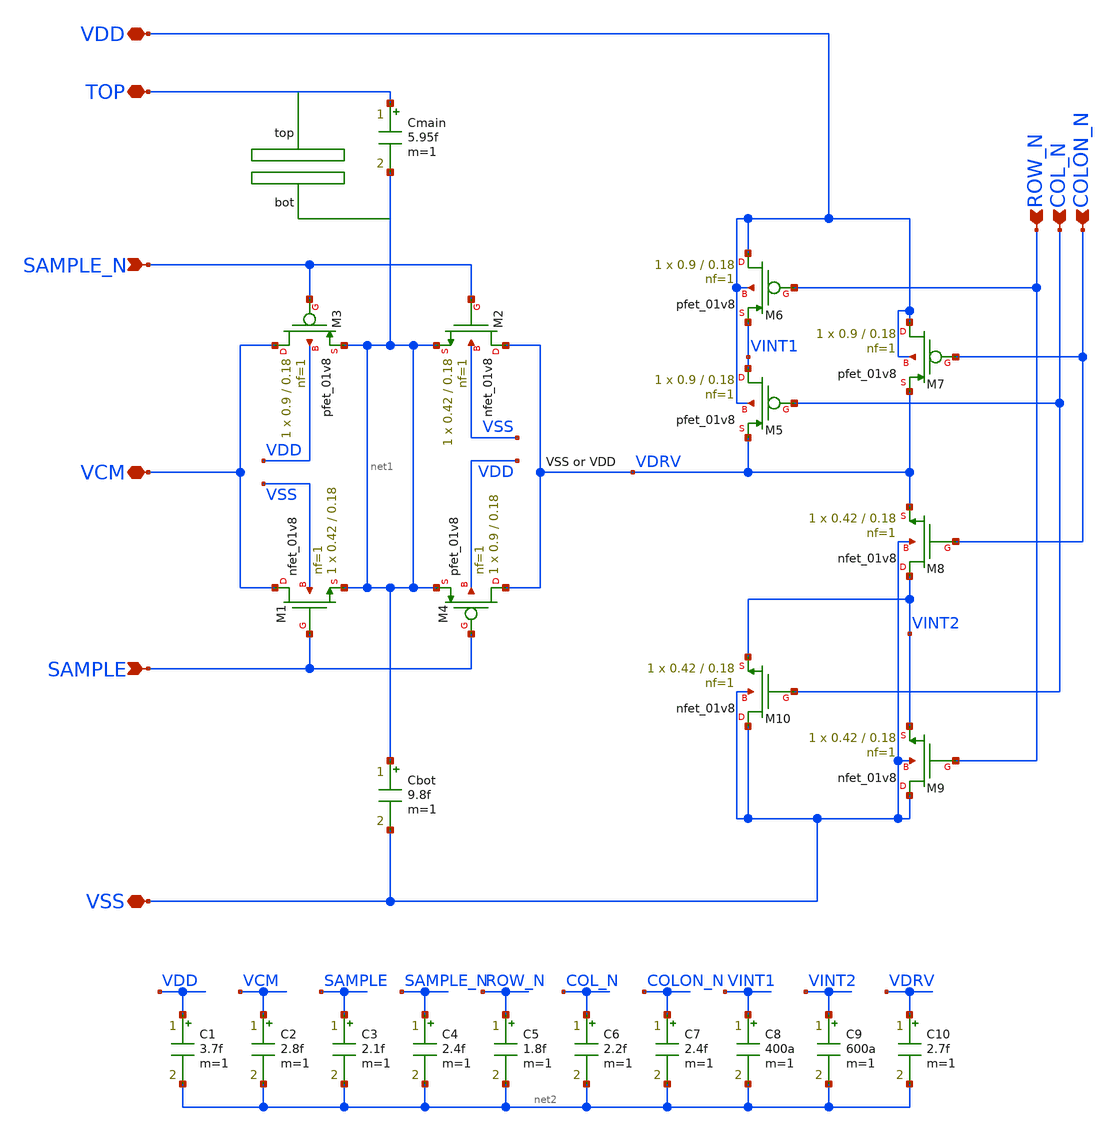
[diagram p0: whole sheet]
** sch_path: xschem/adc_array_cap/adc_array_cap_16.sch
**.subckt adc_array_cap_16 SAMPLE_N SAMPLE VCM ROW_N COL_N COLON_N VDD VSS TOP
*.ipin SAMPLE_N
*.ipin SAMPLE
*.iopin VCM
*.ipin ROW_N
*.ipin COL_N
*.ipin COLON_N
*.iopin VDD
*.iopin VSS
*.iopin TOP
XM1 VCM SAMPLE net1 VSS sky130_fd_pr__nfet_01v8 L=0.18 W=0.42 nf=1 ad='int((nf+1)/2) * W/nf * 0.29' as='int((nf+2)/2) * W/nf * 0.29'
+ pd='2*int((nf+1)/2) * (W/nf + 0.29)' ps='2*int((nf+2)/2) * (W/nf + 0.29)' nrd='0.29 / W' nrs='0.29 / W'
+ sa=0 sb=0 sd=0 mult=1 m=1
XM3 VCM SAMPLE_N net1 VDD sky130_fd_pr__pfet_01v8 L=0.18 W=0.9 nf=1 ad='int((nf+1)/2) * W/nf * 0.29'
+ as='int((nf+2)/2) * W/nf * 0.29' pd='2*int((nf+1)/2) * (W/nf + 0.29)' ps='2*int((nf+2)/2) * (W/nf + 0.29)'
+ nrd='0.29 / W' nrs='0.29 / W' sa=0 sb=0 sd=0 mult=1 m=1
XM2 VDRV SAMPLE_N net1 VSS sky130_fd_pr__nfet_01v8 L=0.18 W=0.42 nf=1 ad='int((nf+1)/2) * W/nf * 0.29'
+ as='int((nf+2)/2) * W/nf * 0.29' pd='2*int((nf+1)/2) * (W/nf + 0.29)' ps='2*int((nf+2)/2) * (W/nf + 0.29)'
+ nrd='0.29 / W' nrs='0.29 / W' sa=0 sb=0 sd=0 mult=1 m=1
XM4 VDRV SAMPLE net1 VDD sky130_fd_pr__pfet_01v8 L=0.18 W=0.9 nf=1 ad='int((nf+1)/2) * W/nf * 0.29' as='int((nf+2)/2) * W/nf * 0.29'
+ pd='2*int((nf+1)/2) * (W/nf + 0.29)' ps='2*int((nf+2)/2) * (W/nf + 0.29)' nrd='0.29 / W' nrs='0.29 / W'
+ sa=0 sb=0 sd=0 mult=1 m=1
XM5 VINT1 COL_N VDRV VDD sky130_fd_pr__pfet_01v8 L=0.18 W=0.9 nf=1 ad='int((nf+1)/2) * W/nf * 0.29' as='int((nf+2)/2) * W/nf * 0.29'
+ pd='2*int((nf+1)/2) * (W/nf + 0.29)' ps='2*int((nf+2)/2) * (W/nf + 0.29)' nrd='0.29 / W' nrs='0.29 / W'
+ sa=0 sb=0 sd=0 mult=1 m=1
XM6 VDD ROW_N VINT1 VDD sky130_fd_pr__pfet_01v8 L=0.18 W=0.9 nf=1 ad='int((nf+1)/2) * W/nf * 0.29' as='int((nf+2)/2) * W/nf * 0.29'
+ pd='2*int((nf+1)/2) * (W/nf + 0.29)' ps='2*int((nf+2)/2) * (W/nf + 0.29)' nrd='0.29 / W' nrs='0.29 / W'
+ sa=0 sb=0 sd=0 mult=1 m=1
XM7 VDD COLON_N VDRV VDD sky130_fd_pr__pfet_01v8 L=0.18 W=0.9 nf=1 ad='int((nf+1)/2) * W/nf * 0.29' as='int((nf+2)/2) * W/nf * 0.29'
+ pd='2*int((nf+1)/2) * (W/nf + 0.29)' ps='2*int((nf+2)/2) * (W/nf + 0.29)' nrd='0.29 / W' nrs='0.29 / W'
+ sa=0 sb=0 sd=0 mult=1 m=1
XM8 VINT2 COLON_N VDRV VSS sky130_fd_pr__nfet_01v8 L=0.18 W=0.42 nf=1 ad='int((nf+1)/2) * W/nf * 0.29'
+ as='int((nf+2)/2) * W/nf * 0.29' pd='2*int((nf+1)/2) * (W/nf + 0.29)' ps='2*int((nf+2)/2) * (W/nf + 0.29)'
+ nrd='0.29 / W' nrs='0.29 / W' sa=0 sb=0 sd=0 mult=1 m=1
XM9 VSS ROW_N VINT2 VSS sky130_fd_pr__nfet_01v8 L=0.18 W=0.42 nf=1 ad='int((nf+1)/2) * W/nf * 0.29' as='int((nf+2)/2) * W/nf * 0.29'
+ pd='2*int((nf+1)/2) * (W/nf + 0.29)' ps='2*int((nf+2)/2) * (W/nf + 0.29)' nrd='0.29 / W' nrs='0.29 / W'
+ sa=0 sb=0 sd=0 mult=1 m=1
XM10 VSS COL_N VINT2 VSS sky130_fd_pr__nfet_01v8 L=0.18 W=0.42 nf=1 ad='int((nf+1)/2) * W/nf * 0.29'
+ as='int((nf+2)/2) * W/nf * 0.29' pd='2*int((nf+1)/2) * (W/nf + 0.29)' ps='2*int((nf+2)/2) * (W/nf + 0.29)'
+ nrd='0.29 / W' nrs='0.29 / W' sa=0 sb=0 sd=0 mult=1 m=1
Cmain TOP net1 5.95f m=1
Cbot net1 VSS 9.8f m=1
C1 VDD net2 3.7f m=1
C2 VCM net2 2.8f m=1
C3 SAMPLE net2 2.1f m=1
C4 SAMPLE_N net2 2.4f m=1
C5 ROW_N net2 1.8f m=1
C6 COL_N net2 2.2f m=1
C7 COLON_N net2 2.4f m=1
C8 VINT1 net2 400a m=1
C9 VINT2 net2 600a m=1
C10 VDRV net2 2.7f m=1
**.ends
.end
